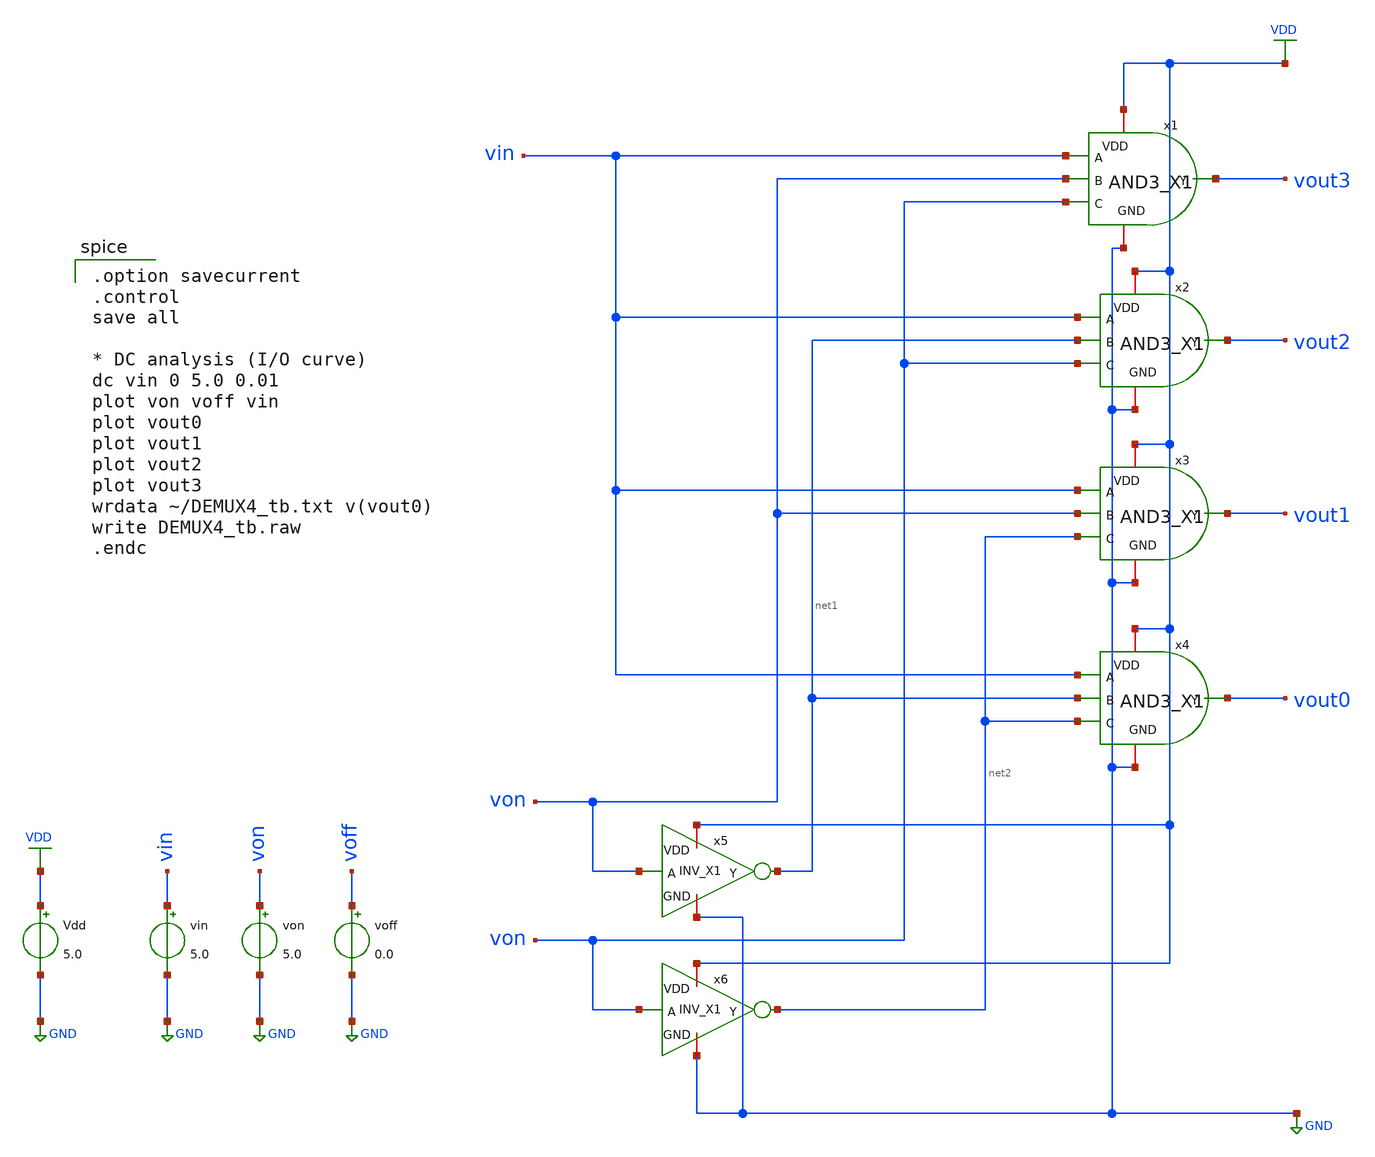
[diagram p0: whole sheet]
** sch_path: member_project/1bit-CPU_ALL/1bit-CPU_MUX_kyushu/DEMUX4_tb.sch
**.subckt DEMUX4_tb
Vdd VDD GND 5.0
von von GND 5.0
voff voff GND 0.0
vin vin GND 5.0
x1 von VDD vout3 vin von GND AND3_X1
x2 von VDD vout2 vin net1 GND AND3_X1
x3 net2 VDD vout1 vin von GND AND3_X1
x4 net2 VDD vout0 vin net1 GND AND3_X1
x5 VDD von net1 GND INV_X1
x6 VDD von net2 GND INV_X1
**** begin user architecture code

.option savecurrent
.control
save all

* DC analysis (I/O curve)
dc vin 0 5.0 0.01
plot von voff vin
plot vout0
plot vout1
plot vout2
plot vout3
wrdata ~/DEMUX4_tb.txt v(vout0)
write DEMUX4_tb.raw
.endc

 .include $::LIB/../ip62_models
**** end user architecture code
**.ends

* expanding   symbol:  IP62_5_stdcell/AND3_X1.sym # of pins=6
** sym_path: IP62_5_stdcell/AND3_X1.sym
** sch_path: IP62_5_stdcell/AND3_X1.sch
.subckt AND3_X1 C VDD Y A B GND
*.opin Y
*.ipin A
*.ipin B
*.iopin VDD
*.iopin GND
*.ipin C
XM4 net1 C VDD VDD PMOS w=10.2u l=1u as=0 ad=0 ps=0 pd=0 nrd=0 nrs=0 m=1
XM2 net1 B VDD VDD PMOS w=10.2u l=1u as=0 ad=0 ps=0 pd=0 nrd=0 nrs=0 m=1
XM3 Y net1 VDD VDD PMOS w=10.2u l=1u as=0 ad=0 ps=0 pd=0 nrd=0 nrs=0 m=1
XM1 VDD A net1 VDD PMOS w=10.2u l=1u as=0 ad=0 ps=0 pd=0 nrd=0 nrs=0 m=1
XM8 Y net1 GND GND NMOS w=3.4u l=1u as=0 ad=0 ps=0 pd=0 nrd=0 nrs=0 m=1
XM5 net1 A net3 GND NMOS w=3.4u l=1u as=0 ad=0 ps=0 pd=0 nrd=0 nrs=0 m=1
XM6 net3 B net2 GND NMOS w=3.4u l=1u as=0 ad=0 ps=0 pd=0 nrd=0 nrs=0 m=1
XM7 net2 C GND GND NMOS w=3.4u l=1u as=0 ad=0 ps=0 pd=0 nrd=0 nrs=0 m=1
.ends


* expanding   symbol:  IP62_5_stdcell/INV_X1.sym # of pins=4
** sym_path: IP62_5_stdcell/INV_X1.sym
** sch_path: IP62_5_stdcell/INV_X1.sch
.subckt INV_X1 VDD A Y GND
*.ipin A
*.opin Y
*.iopin GND
*.iopin VDD
XM7 Y A VDD VDD PMOS w=10.2u l=1u as=0 ad=0 ps=0 pd=0 nrd=0 nrs=0 m=1
XM2 Y A GND GND NMOS w=3.4u l=1u as=0 ad=0 ps=0 pd=0 nrd=0 nrs=0 m=1
.ends

.GLOBAL VDD
.GLOBAL GND
.end
